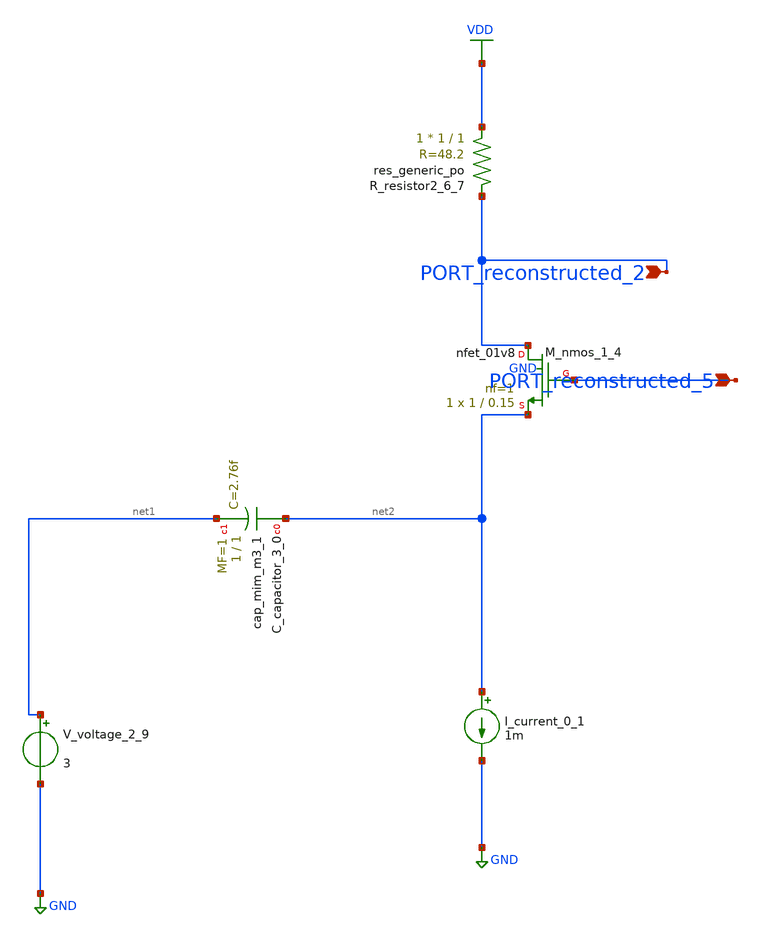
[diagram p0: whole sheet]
** sch_path: schematics/AMSNet/113.sch
**.subckt 113 PORT_reconstructed_5 PORT_reconstructed_2
*.ipin PORT_reconstructed_5
*.ipin PORT_reconstructed_2
XC_capacitor_3_0 net2 net1 sky130_fd_pr__cap_mim_m3_1 W=1 L=1 MF=1 m=1
I_current_0_1 net2 GND 1m
XM_nmos_1_4 PORT_reconstructed_2 PORT_reconstructed_5 net2 GND sky130_fd_pr__nfet_01v8 L=0.15 W=1 nf=1
+ ad='int((1 + 1)/2) * 1 / 1 * 0.29' as='int((1 + 2)/2) * 1 / 1 * 0.29' pd='2*int((1 + 1)/2) * (1 / 1 + 0.29)'
+ ps='2*int((1 + 2)/2) * (1 / 1 + 0.29)' nrd='0.29 / 1 ' nrs='0.29 / 1 ' sa=0 sb=0 sd=0 mult=1 m=1
XR_resistor2_6_7 VDD PORT_reconstructed_2 sky130_fd_pr__res_generic_po W=1 L=1 m=1
V_voltage_2_9 net1 GND 3
**.ends
.GLOBAL GND
.GLOBAL VDD
.end
